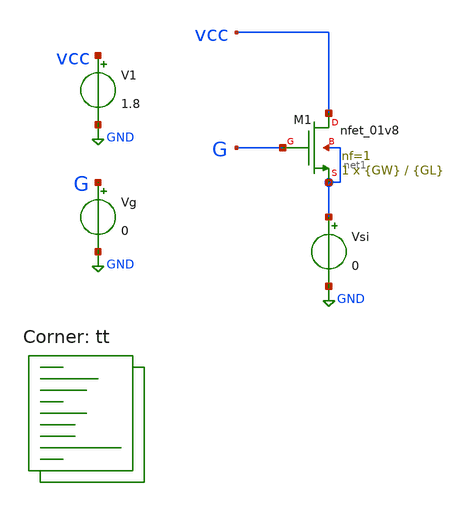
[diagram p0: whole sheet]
** sch_path: xschem/01-nfet-sweep.sch
**.subckt 01-nfet-sweep
XM1 vcc G net1 net1 sky130_fd_pr__nfet_01v8 L={GL} W={GW} nf=1 ad='int((nf+1)/2) * W/nf * 0.29' as='int((nf+2)/2) * W/nf * 0.29'
+ pd='2*int((nf+1)/2) * (W/nf + 0.29)' ps='2*int((nf+2)/2) * (W/nf + 0.29)' nrd='0.29 / W' nrs='0.29 / W'
+ sa=0 sb=0 sd=0 mult=1 m=1
V1 vcc GND 1.8
Vg G GND 0
Vsi net1 GND 0
**** begin user architecture code



.DC Vg 0 1.8 0.01

.param GW = 0.5
.param GL = 0.15

.options savecurrents
.control

  save all
  run
  write 01.raw G i(vsi)

  alterparam GL=0.2
  set appendwrite
  reset
  save all
  run
  write 01.raw G i(vsi)

  alterparam GL=0.25
  set appendwrite
  reset
  save all
  run
  write 01.raw G i(vsi)

  alterparam GL=0.3
  set appendwrite
  reset
  save all
  run
  write 01.raw G i(vsi)

  alterparam GL=0.35
  set appendwrite
  reset
  save all
  run
  write 01.raw G i(vsi)

  alterparam GL=0.4
  set appendwrite
  reset
  save all
  run
  write 01.raw G i(vsi)

  alterparam GL=0.45
  set appendwrite
  reset
  save all
  run
  write 01.raw G i(vsi)

  alterparam GL=0.5
  set appendwrite
  reset
  save all
  run
  write 01.raw G i(vsi)

.endc



.lib $::SKYWATER_MODELS/sky130.lib.spice tt
**** end user architecture code
**.ends
.GLOBAL GND
.end
